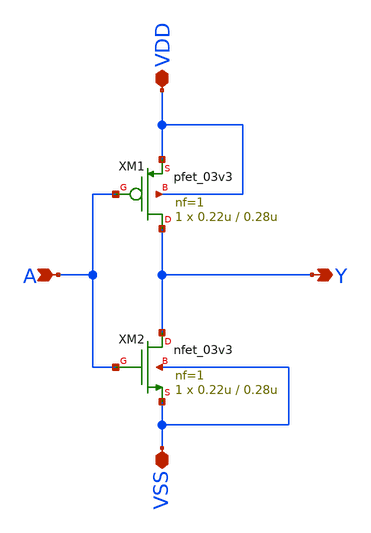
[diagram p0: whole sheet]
** sch_path: inverter.sch
**.subckt inverter A VSS VDD Y
*.ipin A
*.iopin VSS
*.iopin VDD
*.opin Y
XM1 Y A VDD VDD pfet_03v3 L=0.28u W=0.22u nf=1 ad='int((nf+1)/2) * W/nf * 0.18u' as='int((nf+2)/2) * W/nf * 0.18u'
+ pd='2*int((nf+1)/2) * (W/nf + 0.18u)' ps='2*int((nf+2)/2) * (W/nf + 0.18u)' nrd='0.18u / W' nrs='0.18u / W'
+ sa=0 sb=0 sd=0 m=1
XM2 Y A VSS VSS nfet_03v3 L=0.28u W=0.22u nf=1 ad='int((nf+1)/2) * W/nf * 0.18u' as='int((nf+2)/2) * W/nf * 0.18u'
+ pd='2*int((nf+1)/2) * (W/nf + 0.18u)' ps='2*int((nf+2)/2) * (W/nf + 0.18u)' nrd='0.18u / W' nrs='0.18u / W'
+ sa=0 sb=0 sd=0 m=1
**.ends
.end
